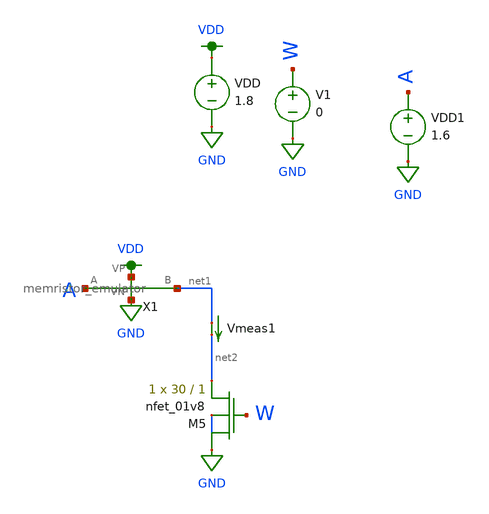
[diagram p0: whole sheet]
** sch_path: schematic/tran_memristor_emulator.sch
**.subckt tran_memristor_emulator
VDD VDD GND 1.8
V1 W GND 0
VDD1 A GND 1.6
Vmeas1 net1 net2 0
.save i(vmeas1)
XM5 GND W net2 GND sky130_fd_pr__nfet_01v8 L=1 W=30 nf=1 ad='int((nf+1)/2) * W/nf * 0.29' as='int((nf+2)/2) * W/nf * 0.29'
+ pd='2*int((nf+1)/2) * (W/nf + 0.29)' ps='2*int((nf+2)/2) * (W/nf + 0.29)' nrd='0.29 / W' nrs='0.29 / W'
+ sa=0 sb=0 sd=0 mult=1 m=1
X1 VDD GND net1 A memristor_emulator
**** begin user architecture code


.control
set wr_vecnames
set wr_singlescale
save all
dc V1 0 1.8 0.01

wrdata ~/neuromorphic_computing_final/simulation/mem.txt i(Vmeas1) v(W)
set appendwrite
.endc



.option wnflag=1
.param MC_SWITCH=0.0
.lib ~/skywater/skywater-pdk/libraries/sky130_fd_pr_ngspice/latest/models/sky130.lib.spice tt

**** end user architecture code
**.ends

* expanding   symbol:  /home/madvlsi/neuromorphic_computing_final/schematic/memristor_emulator.sym #
*+ of pins=4
** sym_path: schematic/memristor_emulator.sym
** sch_path: schematic/memristor_emulator.sch
.subckt memristor_emulator VP VN B A
*.ipin A
*.iopin VN
*.iopin VP
*.opin B
XM1 B net1 A B sky130_fd_pr__pfet_01v8 L=0.35 W=30 nf=1 ad='int((nf+1)/2) * W/nf * 0.29' as='int((nf+2)/2) * W/nf * 0.29'
+ pd='2*int((nf+1)/2) * (W/nf + 0.29)' ps='2*int((nf+2)/2) * (W/nf + 0.29)' nrd='0.29 / W' nrs='0.29 / W'
+ sa=0 sb=0 sd=0 mult=1 m=1
XM2 VP A net1 VP sky130_fd_pr__pfet_01v8 L=2 W=3 nf=1 ad='int((nf+1)/2) * W/nf * 0.29' as='int((nf+2)/2) * W/nf * 0.29'
+ pd='2*int((nf+1)/2) * (W/nf + 0.29)' ps='2*int((nf+2)/2) * (W/nf + 0.29)' nrd='0.29 / W' nrs='0.29 / W'
+ sa=0 sb=0 sd=0 mult=1 m=1
XM3 VN net1 VN VN sky130_fd_pr__nfet_01v8 L=60 W=80 nf=1 ad='int((nf+1)/2) * W/nf * 0.29' as='int((nf+2)/2) * W/nf * 0.29'
+ pd='2*int((nf+1)/2) * (W/nf + 0.29)' ps='2*int((nf+2)/2) * (W/nf + 0.29)' nrd='0.29 / W' nrs='0.29 / W'
+ sa=0 sb=0 sd=0 mult=1 m=1
XM4 VN B net1 VN sky130_fd_pr__nfet_01v8 L=3 W=2 nf=1 ad='int((nf+1)/2) * W/nf * 0.29' as='int((nf+2)/2) * W/nf * 0.29'
+ pd='2*int((nf+1)/2) * (W/nf + 0.29)' ps='2*int((nf+2)/2) * (W/nf + 0.29)' nrd='0.29 / W' nrs='0.29 / W'
+ sa=0 sb=0 sd=0 mult=1 m=1
.ends

.GLOBAL GND
.GLOBAL VDD
.end
